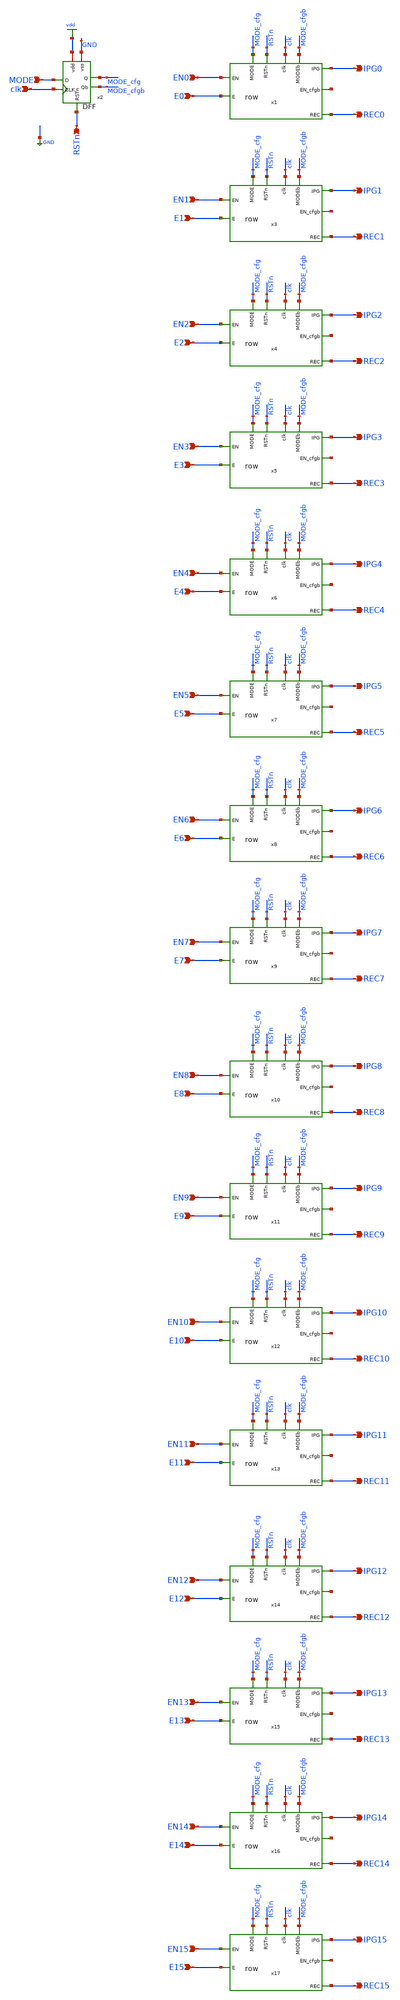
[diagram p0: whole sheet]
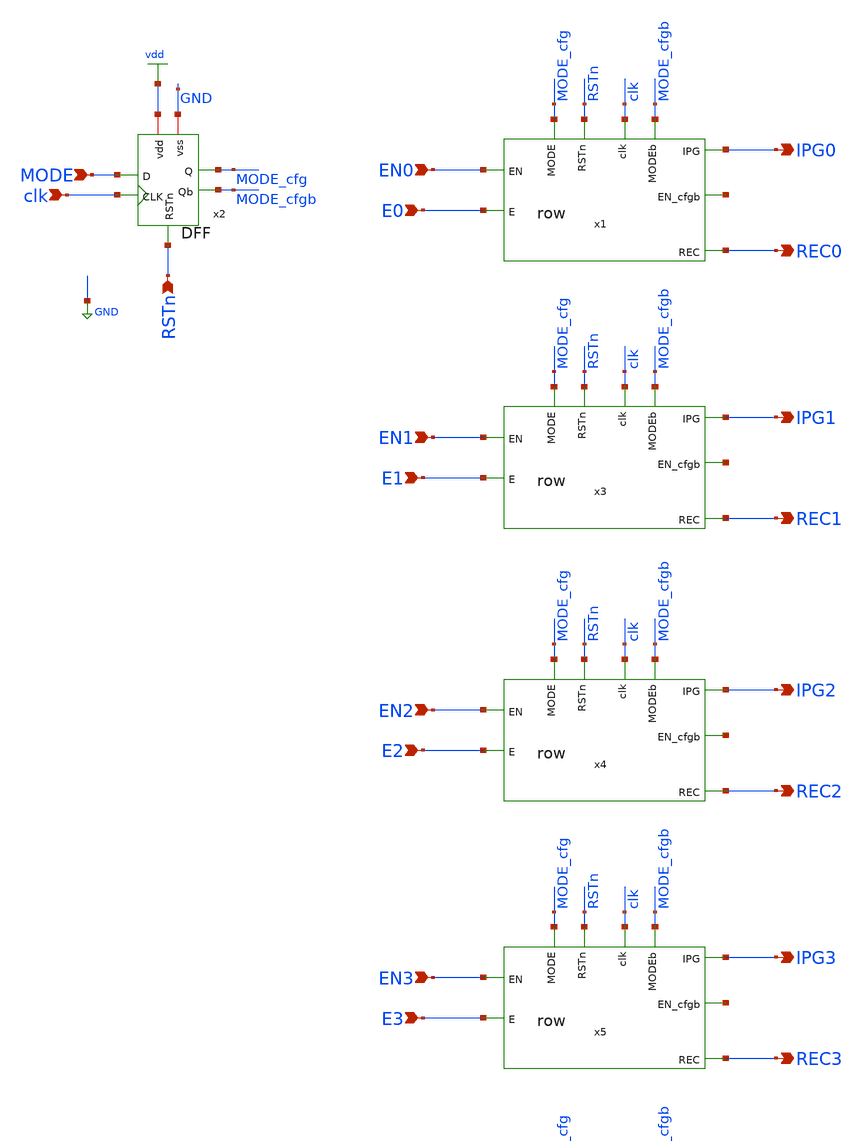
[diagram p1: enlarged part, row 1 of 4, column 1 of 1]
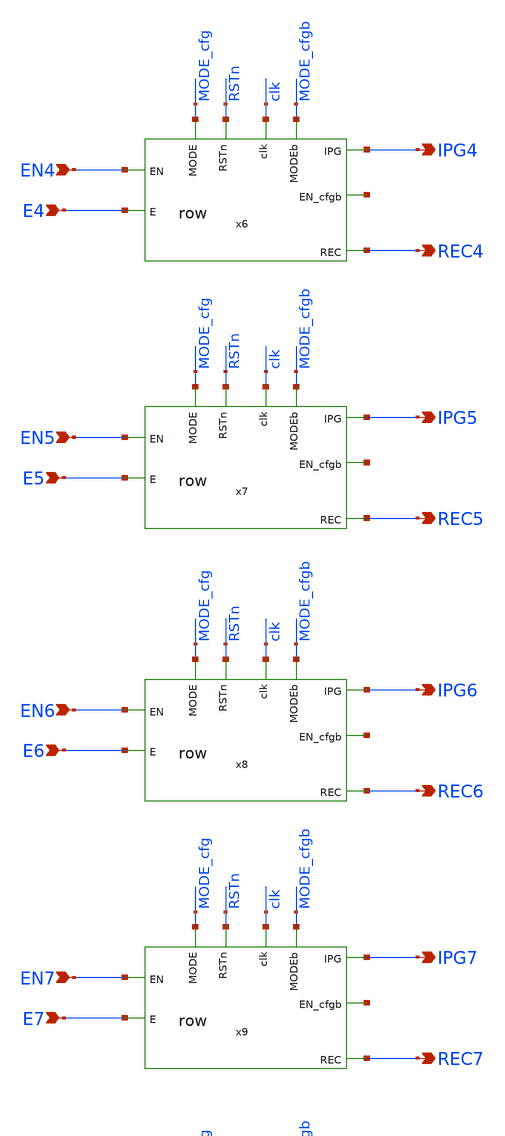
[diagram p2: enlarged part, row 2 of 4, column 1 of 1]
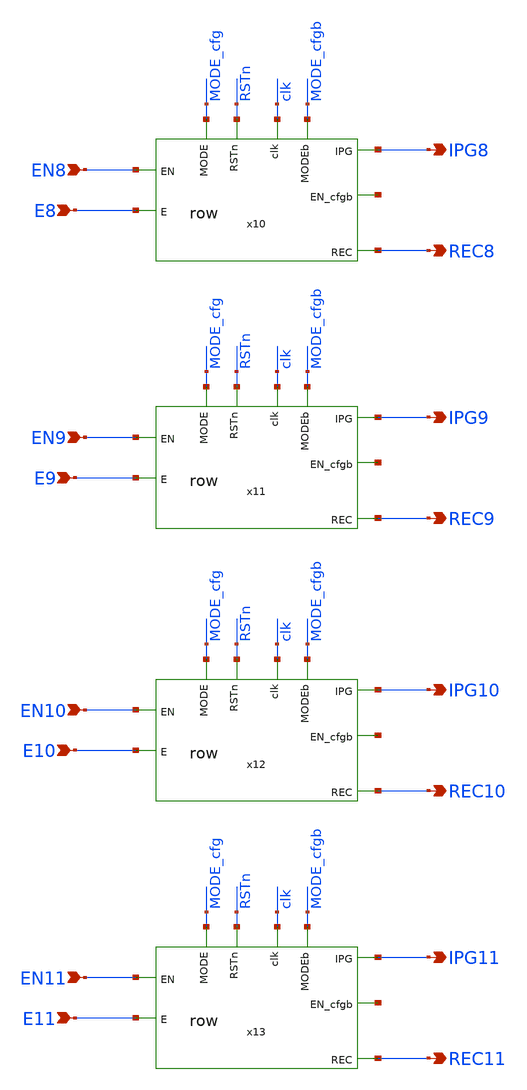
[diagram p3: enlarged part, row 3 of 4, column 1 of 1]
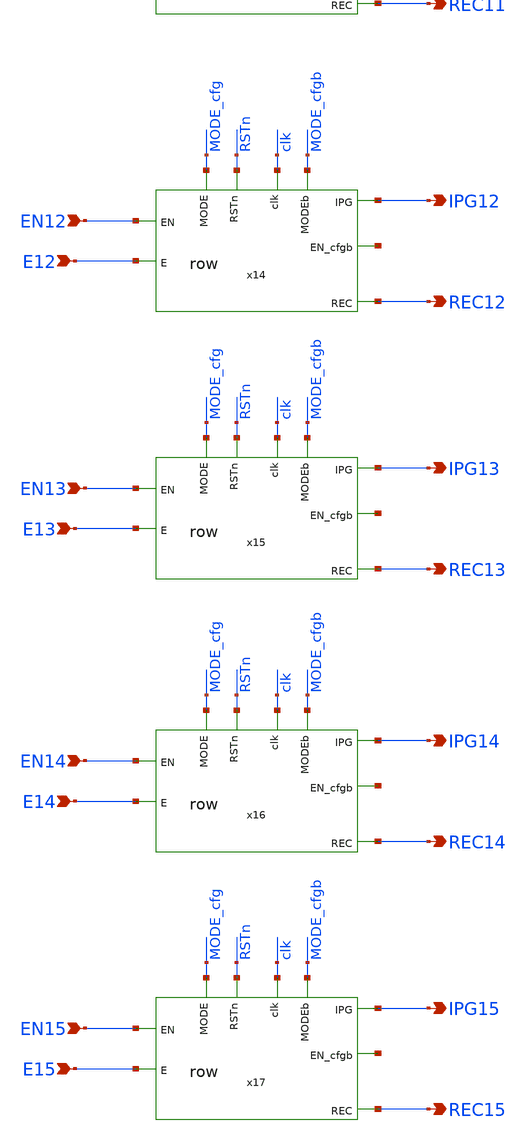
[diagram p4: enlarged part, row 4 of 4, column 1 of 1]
** sch_path: full.sch
**.subckt full RSTn MODE clk EN0 E0 IPG0 REC0 EN1 E1 IPG1 REC1 EN2 E2 IPG2 REC2 EN3 E3 IPG3 REC3 EN4
*+ E4 IPG4 REC4 EN5 E5 IPG5 REC5 EN6 E6 IPG6 REC6 EN7 E7 IPG7 REC7 EN8 E8 IPG8 REC8 EN9 E9 IPG9 REC9 EN10
*+ E10 IPG10 REC10 EN11 E11 IPG11 REC11 EN12 E12 IPG12 REC12 EN13 E13 IPG13 REC13 EN14 E14 IPG14 REC14
*+ EN15 E15 IPG15 REC15
*.ipin RSTn
*.ipin MODE
*.ipin clk
*.ipin EN0
*.ipin E0
*.opin IPG0
*.opin REC0
*.ipin EN1
*.ipin E1
*.opin IPG1
*.opin REC1
*.ipin EN2
*.ipin E2
*.opin IPG2
*.opin REC2
*.ipin EN3
*.ipin E3
*.opin IPG3
*.opin REC3
*.ipin EN4
*.ipin E4
*.opin IPG4
*.opin REC4
*.ipin EN5
*.ipin E5
*.opin IPG5
*.opin REC5
*.ipin EN6
*.ipin E6
*.opin IPG6
*.opin REC6
*.ipin EN7
*.ipin E7
*.opin IPG7
*.opin REC7
*.ipin EN8
*.ipin E8
*.opin IPG8
*.opin REC8
*.ipin EN9
*.ipin E9
*.opin IPG9
*.opin REC9
*.ipin EN10
*.ipin E10
*.opin IPG10
*.opin REC10
*.ipin EN11
*.ipin E11
*.opin IPG11
*.opin REC11
*.ipin EN12
*.ipin E12
*.opin IPG12
*.opin REC12
*.ipin EN13
*.ipin E13
*.opin IPG13
*.opin REC13
*.ipin EN14
*.ipin E14
*.opin IPG14
*.opin REC14
*.ipin EN15
*.ipin E15
*.opin IPG15
*.opin REC15
x1 IPG0 MODE_cfgb EN0 net1 clk E0 MODE_cfg RSTn REC0 row
x2 vdd RSTn MODE MODE_cfg MODE_cfgb clk GND DFF
x3 IPG1 MODE_cfgb EN1 net2 clk E1 MODE_cfg RSTn REC1 row
x4 IPG2 MODE_cfgb EN2 net3 clk E2 MODE_cfg RSTn REC2 row
x5 IPG3 MODE_cfgb EN3 net4 clk E3 MODE_cfg RSTn REC3 row
x6 IPG4 MODE_cfgb EN4 net5 clk E4 MODE_cfg RSTn REC4 row
x7 IPG5 MODE_cfgb EN5 net6 clk E5 MODE_cfg RSTn REC5 row
x8 IPG6 MODE_cfgb EN6 net7 clk E6 MODE_cfg RSTn REC6 row
x9 IPG7 MODE_cfgb EN7 net8 clk E7 MODE_cfg RSTn REC7 row
x10 IPG8 MODE_cfgb EN8 net9 clk E8 MODE_cfg RSTn REC8 row
x11 IPG9 MODE_cfgb EN9 net10 clk E9 MODE_cfg RSTn REC9 row
x12 IPG10 MODE_cfgb EN10 net11 clk E10 MODE_cfg RSTn REC10 row
x13 IPG11 MODE_cfgb EN11 net12 clk E11 MODE_cfg RSTn REC11 row
x14 IPG12 MODE_cfgb EN12 net13 clk E12 MODE_cfg RSTn REC12 row
x15 IPG13 MODE_cfgb EN13 net14 clk E13 MODE_cfg RSTn REC13 row
x16 IPG14 MODE_cfgb EN14 net15 clk E14 MODE_cfg RSTn REC14 row
x17 IPG15 MODE_cfgb EN15 net16 clk E15 MODE_cfg RSTn REC15 row
**.ends

* expanding   symbol:  row.sym # of pins=9
** sym_path: row.sym
** sch_path: row.sch
.subckt row IPG MODEb EN EN_cfgb clk E MODE RSTn REC
*.ipin EN
*.ipin clk
*.ipin MODEb
*.ipin MODE
*.ipin E
*.opin IPG
*.opin REC
*.ipin RSTn
*.opin EN_cfgb
x1 EN_cfg SW_IPG MODEb AND
x2 vdd RSTn EN EN_cfg EN_cfgb clk GND DFF
x3 IPG SW_IPG SW_IPGb E TGATE
x4 EN_cfg SW_REC MODE AND
x6 REC SW_REC SW_RECb E TGATE
x5 SW_IPGb SW_IPG INV
x7 SW_RECb SW_REC INV
.ends


* expanding   symbol:  DFF/DFF.sym # of pins=7
** sym_path: DFF/DFF.sym
** sch_path: DFF/DFF.sch
.subckt DFF vdd RSTn D Q Qb CLK vss
*.ipin D
*.ipin CLK
*.ipin RSTn
*.opin Q
*.iopin vdd
*.iopin vss
*.opin Qb
XM1 net1 D net3 vss nfet_03v3 L=0.28u W=1u nf=1 ad='int((nf+1)/2) * W/nf * 0.18u' as='int((nf+2)/2) * W/nf * 0.18u'
+ pd='2*int((nf+1)/2) * (W/nf + 0.18u)' ps='2*int((nf+2)/2) * (W/nf + 0.18u)' nrd='0.18u / W' nrs='0.18u / W'
+ sa=0 sb=0 sd=0 m=1
XM2 net1 D net2 vdd pfet_03v3 L=0.28u W=1u nf=1 ad='int((nf+1)/2) * W/nf * 0.18u' as='int((nf+2)/2) * W/nf * 0.18u'
+ pd='2*int((nf+1)/2) * (W/nf + 0.18u)' ps='2*int((nf+2)/2) * (W/nf + 0.18u)' nrd='0.18u / W' nrs='0.18u / W'
+ sa=0 sb=0 sd=0 m=1
XM3 net2 c vdd vdd pfet_03v3 L=0.28u W=1u nf=1 ad='int((nf+1)/2) * W/nf * 0.18u' as='int((nf+2)/2) * W/nf * 0.18u'
+ pd='2*int((nf+1)/2) * (W/nf + 0.18u)' ps='2*int((nf+2)/2) * (W/nf + 0.18u)' nrd='0.18u / W' nrs='0.18u / W'
+ sa=0 sb=0 sd=0 m=1
XM4 net3 cbar vss vss nfet_03v3 L=0.28u W=1u nf=1 ad='int((nf+1)/2) * W/nf * 0.18u' as='int((nf+2)/2) * W/nf * 0.18u'
+ pd='2*int((nf+1)/2) * (W/nf + 0.18u)' ps='2*int((nf+2)/2) * (W/nf + 0.18u)' nrd='0.18u / W' nrs='0.18u / W'
+ sa=0 sb=0 sd=0 m=1
XM5 cbar CLK vss vss nfet_03v3 L=0.28u W=1u nf=1 ad='int((nf+1)/2) * W/nf * 0.18u' as='int((nf+2)/2) * W/nf * 0.18u'
+ pd='2*int((nf+1)/2) * (W/nf + 0.18u)' ps='2*int((nf+2)/2) * (W/nf + 0.18u)' nrd='0.18u / W' nrs='0.18u / W'
+ sa=0 sb=0 sd=0 m=1
XM6 cbar CLK vdd vdd pfet_03v3 L=0.28u W=1u nf=1 ad='int((nf+1)/2) * W/nf * 0.18u' as='int((nf+2)/2) * W/nf * 0.18u'
+ pd='2*int((nf+1)/2) * (W/nf + 0.18u)' ps='2*int((nf+2)/2) * (W/nf + 0.18u)' nrd='0.18u / W' nrs='0.18u / W'
+ sa=0 sb=0 sd=0 m=1
XM7 c cbar vss vss nfet_03v3 L=0.28u W=1u nf=1 ad='int((nf+1)/2) * W/nf * 0.18u' as='int((nf+2)/2) * W/nf * 0.18u'
+ pd='2*int((nf+1)/2) * (W/nf + 0.18u)' ps='2*int((nf+2)/2) * (W/nf + 0.18u)' nrd='0.18u / W' nrs='0.18u / W'
+ sa=0 sb=0 sd=0 m=1
XM8 c cbar vdd vdd pfet_03v3 L=0.28u W=1u nf=1 ad='int((nf+1)/2) * W/nf * 0.18u' as='int((nf+2)/2) * W/nf * 0.18u'
+ pd='2*int((nf+1)/2) * (W/nf + 0.18u)' ps='2*int((nf+2)/2) * (W/nf + 0.18u)' nrd='0.18u / W' nrs='0.18u / W'
+ sa=0 sb=0 sd=0 m=1
XM11 net5 RSTn net4 vss nfet_03v3 L=0.28u W=1u nf=1 ad='int((nf+1)/2) * W/nf * 0.18u' as='int((nf+2)/2) * W/nf * 0.18u'
+ pd='2*int((nf+1)/2) * (W/nf + 0.18u)' ps='2*int((nf+2)/2) * (W/nf + 0.18u)' nrd='0.18u / W' nrs='0.18u / W'
+ sa=0 sb=0 sd=0 m=1
XM12 net4 net6 vss vss nfet_03v3 L=0.28u W=1u nf=1 ad='int((nf+1)/2) * W/nf * 0.18u' as='int((nf+2)/2) * W/nf * 0.18u'
+ pd='2*int((nf+1)/2) * (W/nf + 0.18u)' ps='2*int((nf+2)/2) * (W/nf + 0.18u)' nrd='0.18u / W' nrs='0.18u / W'
+ sa=0 sb=0 sd=0 m=1
XM13 net5 RSTn vdd vdd pfet_03v3 L=0.28u W=1u nf=1 ad='int((nf+1)/2) * W/nf * 0.18u' as='int((nf+2)/2) * W/nf * 0.18u'
+ pd='2*int((nf+1)/2) * (W/nf + 0.18u)' ps='2*int((nf+2)/2) * (W/nf + 0.18u)' nrd='0.18u / W' nrs='0.18u / W'
+ sa=0 sb=0 sd=0 m=1
XM14 net5 net6 vdd vdd pfet_03v3 L=0.28u W=1u nf=1 ad='int((nf+1)/2) * W/nf * 0.18u' as='int((nf+2)/2) * W/nf * 0.18u'
+ pd='2*int((nf+1)/2) * (W/nf + 0.18u)' ps='2*int((nf+2)/2) * (W/nf + 0.18u)' nrd='0.18u / W' nrs='0.18u / W'
+ sa=0 sb=0 sd=0 m=1
XM15 net6 net1 vss vss nfet_03v3 L=0.28u W=1u nf=1 ad='int((nf+1)/2) * W/nf * 0.18u' as='int((nf+2)/2) * W/nf * 0.18u'
+ pd='2*int((nf+1)/2) * (W/nf + 0.18u)' ps='2*int((nf+2)/2) * (W/nf + 0.18u)' nrd='0.18u / W' nrs='0.18u / W'
+ sa=0 sb=0 sd=0 m=1
XM16 net6 net1 vdd vdd pfet_03v3 L=0.28u W=1u nf=1 ad='int((nf+1)/2) * W/nf * 0.18u' as='int((nf+2)/2) * W/nf * 0.18u'
+ pd='2*int((nf+1)/2) * (W/nf + 0.18u)' ps='2*int((nf+2)/2) * (W/nf + 0.18u)' nrd='0.18u / W' nrs='0.18u / W'
+ sa=0 sb=0 sd=0 m=1
XM21 net9 net7 net8 vss nfet_03v3 L=0.28u W=1u nf=1 ad='int((nf+1)/2) * W/nf * 0.18u' as='int((nf+2)/2) * W/nf * 0.18u'
+ pd='2*int((nf+1)/2) * (W/nf + 0.18u)' ps='2*int((nf+2)/2) * (W/nf + 0.18u)' nrd='0.18u / W' nrs='0.18u / W'
+ sa=0 sb=0 sd=0 m=1
XM22 net8 RSTn vss vss nfet_03v3 L=0.28u W=1u nf=1 ad='int((nf+1)/2) * W/nf * 0.18u' as='int((nf+2)/2) * W/nf * 0.18u'
+ pd='2*int((nf+1)/2) * (W/nf + 0.18u)' ps='2*int((nf+2)/2) * (W/nf + 0.18u)' nrd='0.18u / W' nrs='0.18u / W'
+ sa=0 sb=0 sd=0 m=1
XM23 net9 net7 vdd vdd pfet_03v3 L=0.28u W=1u nf=1 ad='int((nf+1)/2) * W/nf * 0.18u' as='int((nf+2)/2) * W/nf * 0.18u'
+ pd='2*int((nf+1)/2) * (W/nf + 0.18u)' ps='2*int((nf+2)/2) * (W/nf + 0.18u)' nrd='0.18u / W' nrs='0.18u / W'
+ sa=0 sb=0 sd=0 m=1
XM24 net9 RSTn vdd vdd pfet_03v3 L=0.28u W=1u nf=1 ad='int((nf+1)/2) * W/nf * 0.18u' as='int((nf+2)/2) * W/nf * 0.18u'
+ pd='2*int((nf+1)/2) * (W/nf + 0.18u)' ps='2*int((nf+2)/2) * (W/nf + 0.18u)' nrd='0.18u / W' nrs='0.18u / W'
+ sa=0 sb=0 sd=0 m=1
XM25 Q net9 vss vss nfet_03v3 L=0.28u W=1u nf=1 ad='int((nf+1)/2) * W/nf * 0.18u' as='int((nf+2)/2) * W/nf * 0.18u'
+ pd='2*int((nf+1)/2) * (W/nf + 0.18u)' ps='2*int((nf+2)/2) * (W/nf + 0.18u)' nrd='0.18u / W' nrs='0.18u / W'
+ sa=0 sb=0 sd=0 m=1
XM26 Q net9 vdd vdd pfet_03v3 L=0.28u W=1u nf=1 ad='int((nf+1)/2) * W/nf * 0.18u' as='int((nf+2)/2) * W/nf * 0.18u'
+ pd='2*int((nf+1)/2) * (W/nf + 0.18u)' ps='2*int((nf+2)/2) * (W/nf + 0.18u)' nrd='0.18u / W' nrs='0.18u / W'
+ sa=0 sb=0 sd=0 m=1
XM19 net7 net9 net11 vss nfet_03v3 L=0.28u W=1u nf=1 ad='int((nf+1)/2) * W/nf * 0.18u' as='int((nf+2)/2) * W/nf * 0.18u'
+ pd='2*int((nf+1)/2) * (W/nf + 0.18u)' ps='2*int((nf+2)/2) * (W/nf + 0.18u)' nrd='0.18u / W' nrs='0.18u / W'
+ sa=0 sb=0 sd=0 m=1
XM20 net7 net9 net10 vdd pfet_03v3 L=0.28u W=1u nf=1 ad='int((nf+1)/2) * W/nf * 0.18u' as='int((nf+2)/2) * W/nf * 0.18u'
+ pd='2*int((nf+1)/2) * (W/nf + 0.18u)' ps='2*int((nf+2)/2) * (W/nf + 0.18u)' nrd='0.18u / W' nrs='0.18u / W'
+ sa=0 sb=0 sd=0 m=1
XM31 net10 c vdd vdd pfet_03v3 L=0.28u W=1u nf=1 ad='int((nf+1)/2) * W/nf * 0.18u' as='int((nf+2)/2) * W/nf * 0.18u'
+ pd='2*int((nf+1)/2) * (W/nf + 0.18u)' ps='2*int((nf+2)/2) * (W/nf + 0.18u)' nrd='0.18u / W' nrs='0.18u / W'
+ sa=0 sb=0 sd=0 m=1
XM32 net11 cbar vss vss nfet_03v3 L=0.28u W=1u nf=1 ad='int((nf+1)/2) * W/nf * 0.18u' as='int((nf+2)/2) * W/nf * 0.18u'
+ pd='2*int((nf+1)/2) * (W/nf + 0.18u)' ps='2*int((nf+2)/2) * (W/nf + 0.18u)' nrd='0.18u / W' nrs='0.18u / W'
+ sa=0 sb=0 sd=0 m=1
XM35 net12 net9 vss vss nfet_03v3 L=0.28u W=1u nf=1 ad='int((nf+1)/2) * W/nf * 0.18u' as='int((nf+2)/2) * W/nf * 0.18u'
+ pd='2*int((nf+1)/2) * (W/nf + 0.18u)' ps='2*int((nf+2)/2) * (W/nf + 0.18u)' nrd='0.18u / W' nrs='0.18u / W'
+ sa=0 sb=0 sd=0 m=1
XM36 net12 net9 vdd vdd pfet_03v3 L=0.28u W=1u nf=1 ad='int((nf+1)/2) * W/nf * 0.18u' as='int((nf+2)/2) * W/nf * 0.18u'
+ pd='2*int((nf+1)/2) * (W/nf + 0.18u)' ps='2*int((nf+2)/2) * (W/nf + 0.18u)' nrd='0.18u / W' nrs='0.18u / W'
+ sa=0 sb=0 sd=0 m=1
XM37 Qb net12 vss vss nfet_03v3 L=0.28u W=1u nf=1 ad='int((nf+1)/2) * W/nf * 0.18u' as='int((nf+2)/2) * W/nf * 0.18u'
+ pd='2*int((nf+1)/2) * (W/nf + 0.18u)' ps='2*int((nf+2)/2) * (W/nf + 0.18u)' nrd='0.18u / W' nrs='0.18u / W'
+ sa=0 sb=0 sd=0 m=1
XM38 Qb net12 vdd vdd pfet_03v3 L=0.28u W=1u nf=1 ad='int((nf+1)/2) * W/nf * 0.18u' as='int((nf+2)/2) * W/nf * 0.18u'
+ pd='2*int((nf+1)/2) * (W/nf + 0.18u)' ps='2*int((nf+2)/2) * (W/nf + 0.18u)' nrd='0.18u / W' nrs='0.18u / W'
+ sa=0 sb=0 sd=0 m=1
XM9 net1 c net5 vss nfet_03v3 L=0.28u W=1u nf=1 ad='int((nf+1)/2) * W/nf * 0.18u' as='int((nf+2)/2) * W/nf * 0.18u'
+ pd='2*int((nf+1)/2) * (W/nf + 0.18u)' ps='2*int((nf+2)/2) * (W/nf + 0.18u)' nrd='0.18u / W' nrs='0.18u / W'
+ sa=0 sb=0 sd=0 m=1
XM10 net1 cbar net5 vdd pfet_03v3 L=0.28u W=1u nf=1 ad='int((nf+1)/2) * W/nf * 0.18u' as='int((nf+2)/2) * W/nf * 0.18u'
+ pd='2*int((nf+1)/2) * (W/nf + 0.18u)' ps='2*int((nf+2)/2) * (W/nf + 0.18u)' nrd='0.18u / W' nrs='0.18u / W'
+ sa=0 sb=0 sd=0 m=1
XM17 net6 c net7 vss nfet_03v3 L=0.28u W=1u nf=1 ad='int((nf+1)/2) * W/nf * 0.18u' as='int((nf+2)/2) * W/nf * 0.18u'
+ pd='2*int((nf+1)/2) * (W/nf + 0.18u)' ps='2*int((nf+2)/2) * (W/nf + 0.18u)' nrd='0.18u / W' nrs='0.18u / W'
+ sa=0 sb=0 sd=0 m=1
XM18 net6 cbar net7 vdd pfet_03v3 L=0.28u W=1u nf=1 ad='int((nf+1)/2) * W/nf * 0.18u' as='int((nf+2)/2) * W/nf * 0.18u'
+ pd='2*int((nf+1)/2) * (W/nf + 0.18u)' ps='2*int((nf+2)/2) * (W/nf + 0.18u)' nrd='0.18u / W' nrs='0.18u / W'
+ sa=0 sb=0 sd=0 m=1
.ends


* expanding   symbol:  AND/AND.sym # of pins=3
** sym_path: AND/AND.sym
** sch_path: AND/AND.sch
.subckt AND IN0 OUT IN1
*.opin OUT
*.ipin IN0
*.ipin IN1
XM1 net1 IN0 net2 GND nfet_03v3 L=0.28u W=1u nf=1 ad='int((nf+1)/2) * W/nf * 0.18u' as='int((nf+2)/2) * W/nf * 0.18u'
+ pd='2*int((nf+1)/2) * (W/nf + 0.18u)' ps='2*int((nf+2)/2) * (W/nf + 0.18u)' nrd='0.18u / W' nrs='0.18u / W'
+ sa=0 sb=0 sd=0 m=1
XM2 net2 IN1 GND GND nfet_03v3 L=0.28u W=1u nf=1 ad='int((nf+1)/2) * W/nf * 0.18u' as='int((nf+2)/2) * W/nf * 0.18u'
+ pd='2*int((nf+1)/2) * (W/nf + 0.18u)' ps='2*int((nf+2)/2) * (W/nf + 0.18u)' nrd='0.18u / W' nrs='0.18u / W'
+ sa=0 sb=0 sd=0 m=1
XM3 net1 IN0 vdd vdd pfet_03v3 L=0.28u W=1u nf=1 ad='int((nf+1)/2) * W/nf * 0.18u' as='int((nf+2)/2) * W/nf * 0.18u'
+ pd='2*int((nf+1)/2) * (W/nf + 0.18u)' ps='2*int((nf+2)/2) * (W/nf + 0.18u)' nrd='0.18u / W' nrs='0.18u / W'
+ sa=0 sb=0 sd=0 m=1
XM4 net1 IN1 vdd vdd pfet_03v3 L=0.28u W=1u nf=1 ad='int((nf+1)/2) * W/nf * 0.18u' as='int((nf+2)/2) * W/nf * 0.18u'
+ pd='2*int((nf+1)/2) * (W/nf + 0.18u)' ps='2*int((nf+2)/2) * (W/nf + 0.18u)' nrd='0.18u / W' nrs='0.18u / W'
+ sa=0 sb=0 sd=0 m=1
x1 OUT net1 INV
.ends


* expanding   symbol:  TGATE/TGATE.sym # of pins=4
** sym_path: TGATE/TGATE.sym
** sch_path: TGATE/TGATE.sch
.subckt TGATE out c cbar in
*.ipin in
*.opin out
*.ipin cbar
*.ipin c
XM1 out cbar in VDD pfet_03v3 L=0.28u W=1u nf=1 ad='int((nf+1)/2) * W/nf * 0.18u' as='int((nf+2)/2) * W/nf * 0.18u'
+ pd='2*int((nf+1)/2) * (W/nf + 0.18u)' ps='2*int((nf+2)/2) * (W/nf + 0.18u)' nrd='0.18u / W' nrs='0.18u / W'
+ sa=0 sb=0 sd=0 m=1
XM2 out c in GND nfet_03v3 L=0.28u W=1u nf=1 ad='int((nf+1)/2) * W/nf * 0.18u' as='int((nf+2)/2) * W/nf * 0.18u'
+ pd='2*int((nf+1)/2) * (W/nf + 0.18u)' ps='2*int((nf+2)/2) * (W/nf + 0.18u)' nrd='0.18u / W' nrs='0.18u / W'
+ sa=0 sb=0 sd=0 m=1
.ends


* expanding   symbol:  AND/INV.sym # of pins=2
** sym_path: AND/INV.sym
** sch_path: AND/INV.sch
.subckt INV OUT IN
*.ipin IN
*.opin OUT
XM1 OUT IN VDD VDD pfet_03v3 L=0.28u W=1u nf=1 ad='int((nf+1)/2) * W/nf * 0.18u' as='int((nf+2)/2) * W/nf * 0.18u'
+ pd='2*int((nf+1)/2) * (W/nf + 0.18u)' ps='2*int((nf+2)/2) * (W/nf + 0.18u)' nrd='0.18u / W' nrs='0.18u / W'
+ sa=0 sb=0 sd=0 m=1
XM2 OUT IN GND GND nfet_03v3 L=0.28u W=0.5u nf=1 ad='int((nf+1)/2) * W/nf * 0.18u' as='int((nf+2)/2) * W/nf * 0.18u'
+ pd='2*int((nf+1)/2) * (W/nf + 0.18u)' ps='2*int((nf+2)/2) * (W/nf + 0.18u)' nrd='0.18u / W' nrs='0.18u / W'
+ sa=0 sb=0 sd=0 m=1
.ends

.GLOBAL GND
.GLOBAL vdd
.GLOBAL VDD
.end
